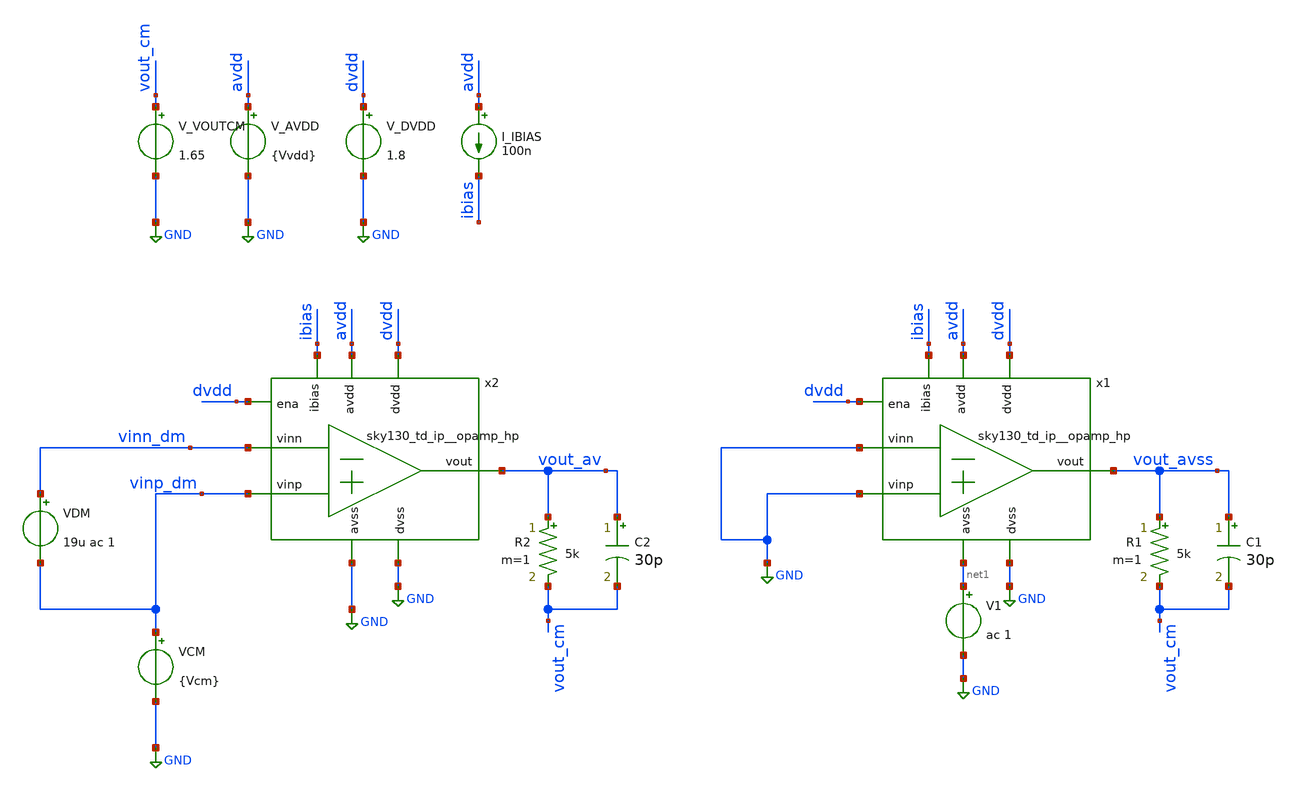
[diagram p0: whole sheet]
** sch_path: cace/psrrn.sch
**.subckt psrrn
x1 avdd vout_avss ibias GND GND net1 dvdd GND dvdd sky130_td_ip__opamp_hp
V_AVDD avdd GND {Vvdd}
.save i(v_avdd)
V_DVDD dvdd GND 1.8
.save i(v_dvdd)
I_IBIAS avdd ibias 100n
R1 vout_avss vout_cm 5k m=1
C1 vout_avss vout_cm 30p m=1
V_VOUTCM vout_cm GND 1.65
.save i(v_voutcm)
V1 net1 GND ac 1
x2 avdd vout_av ibias vinn_dm vinp_dm GND dvdd GND dvdd sky130_td_ip__opamp_hp
R2 vout_av vout_cm 5k m=1
C2 vout_av vout_cm 30p m=1
VDM vinn_dm vinp_dm 19u ac 1
VCM vinp_dm GND {Vcm}
.save i(vcm)
**** begin user architecture code


.save all

.control
save all

* Calculate input offset voltage
alter VDM pwl = [ 0 -10m 10 10m ]
tran 10m 10
run
let vid = v(vinn_dm) - v(vinp_dm)
let vout = v(vout_av)
meas tran input_offset_voltage FIND vid WHEN vout=1.65

alter @VDM[pwl] = [ 0 0 ]
alter VDM dc = $&input_offset_voltage
alter VDM ac = 1

* Run AC sweep from 1Hz to 1GHz
AC DEC 100 1 1000000000
run

* Get DC gain in DBs.
let av_db = db(vout_av)
let avss_db = db(vout_avss)
let psrrn_db = av_db - avss_db

meas AC psrrn_dc FIND psrrn_db AT=1
meas AC psrrn_10k FIND psrrn_db AT=10K

echo
echo ===================================
echo PSRR- characterization results:
echo - PSRR @ 1 Hz: $&psrrn_dc
echo - PSRR @ 10 kHz: $&psrrn_10k
echo ===================================


echo $&psrrn_dc $&psrrn_10k > {simpath}/{filename}_{N}.data
quit
.endc




* CACE gensim simulation file {filename}_{N}
* Generated by CACE gensim, Efabless Corporation (c) 2023
* Find the power supply rejection ratio of the amplifier

.include {DUT_path}

.lib {PDK_ROOT}/{PDK}/libs.tech/combined/sky130.lib.spice {corner}

.option TEMP={temperature}
* Flag unsafe operating conditions (exceeds models' specified limits)
.option warn=1
.option SEED=[{seed=12345} + {iterations=0}]


**** end user architecture code
**.ends
.GLOBAL GND
.end
